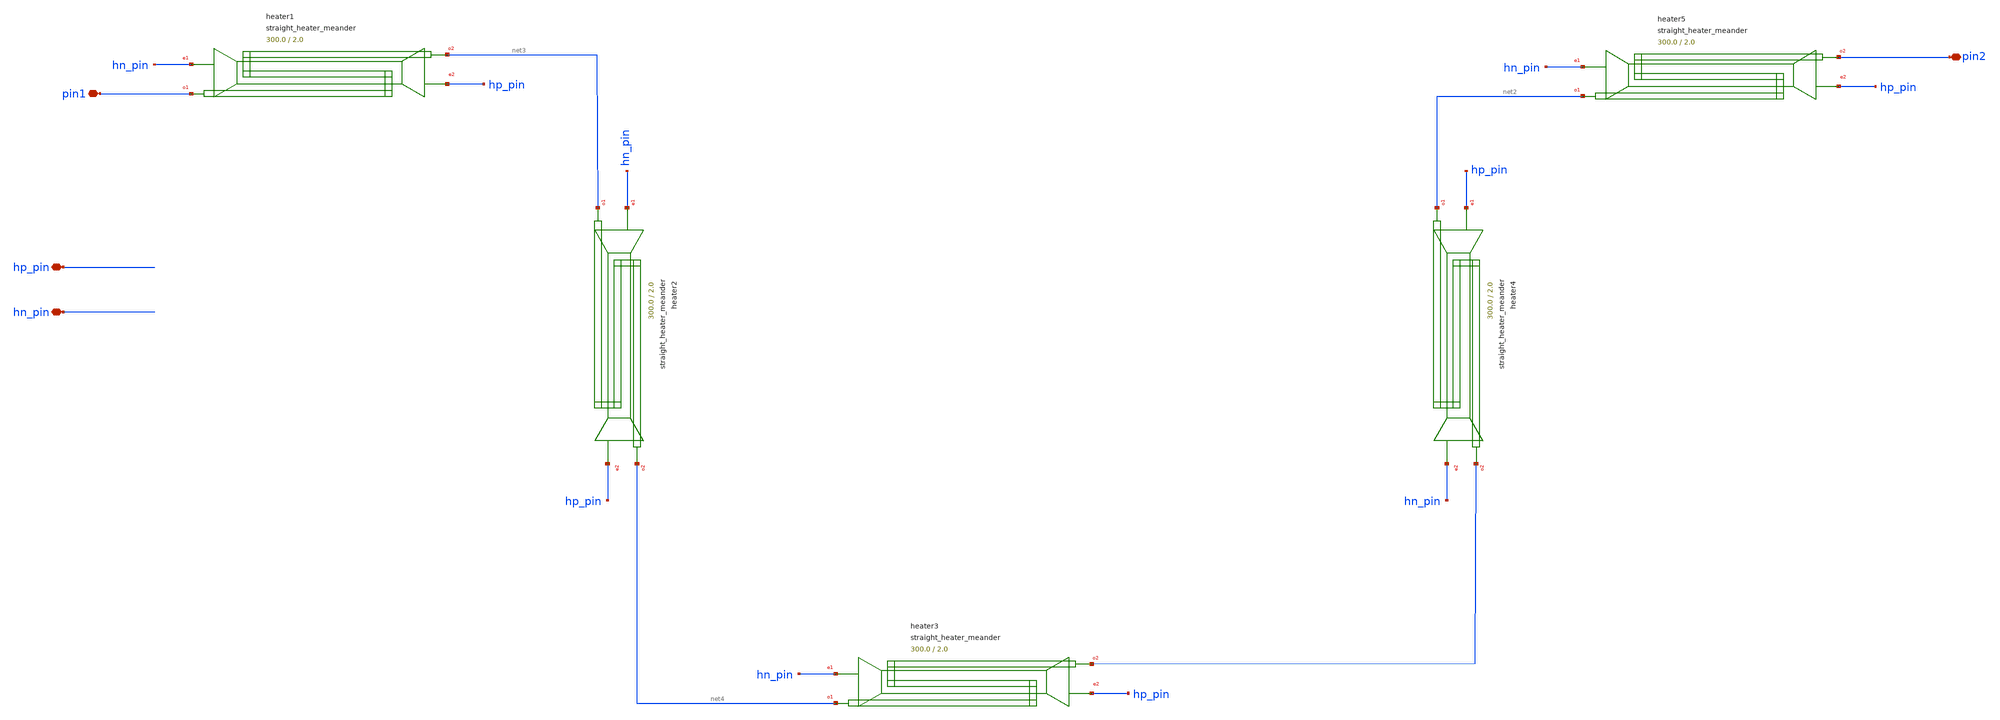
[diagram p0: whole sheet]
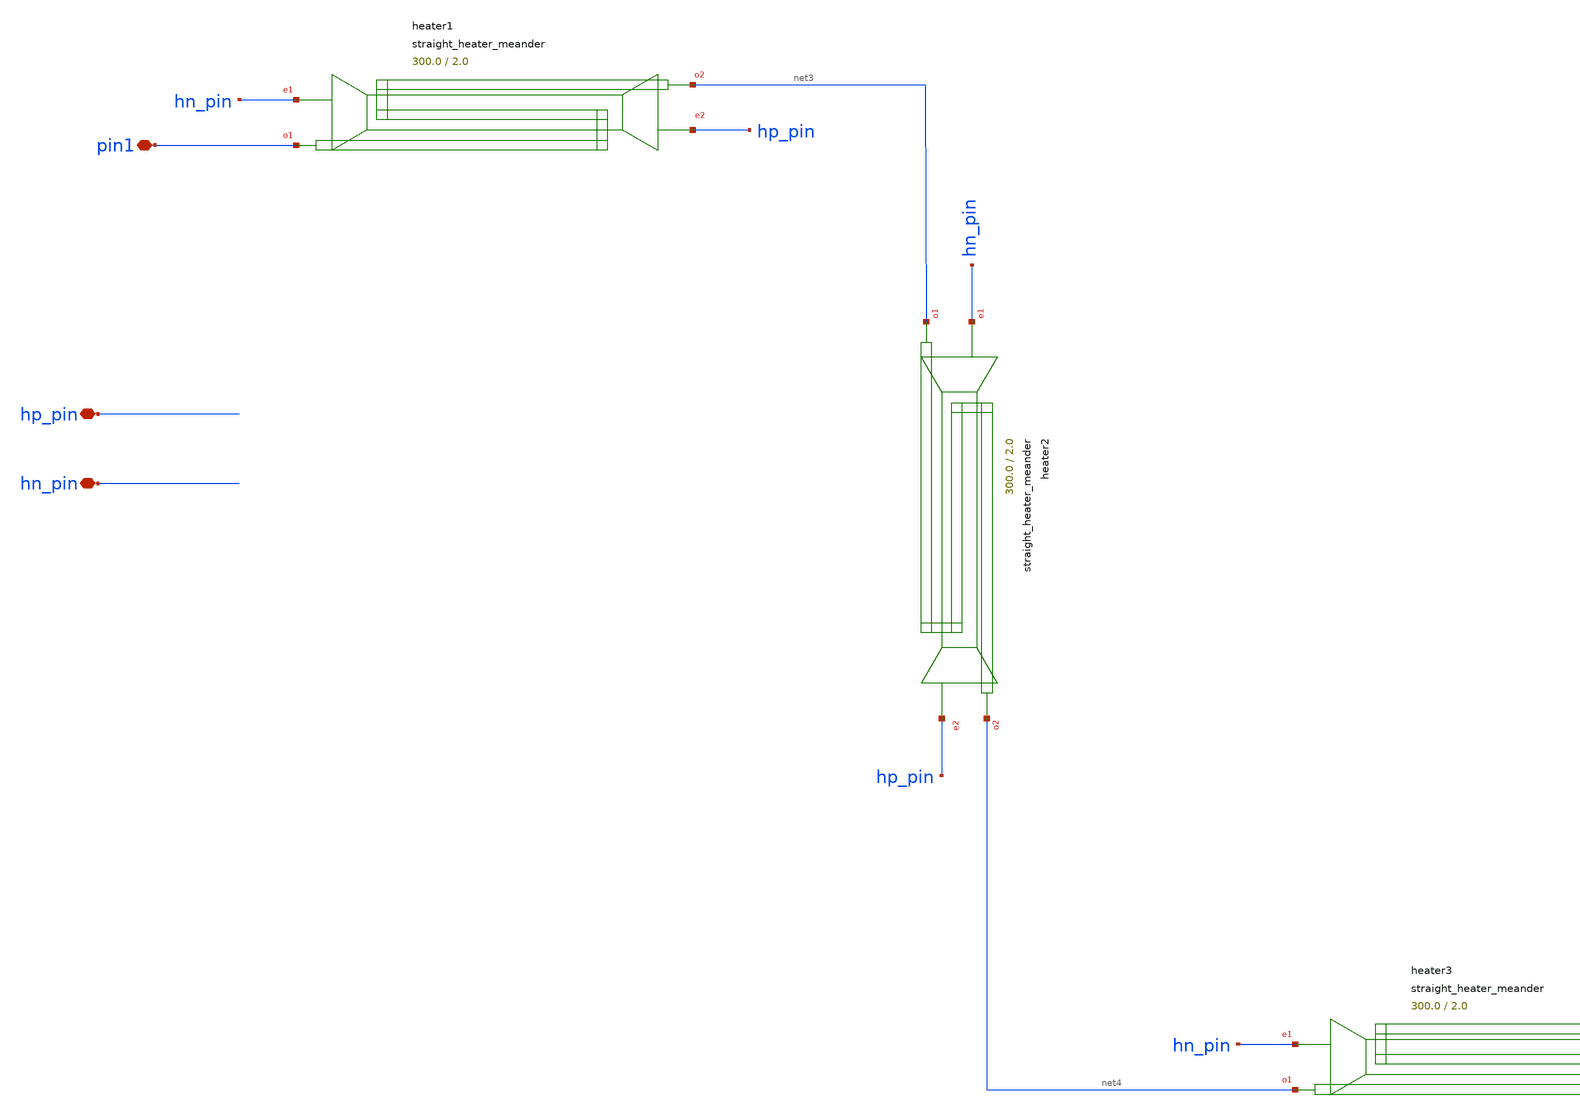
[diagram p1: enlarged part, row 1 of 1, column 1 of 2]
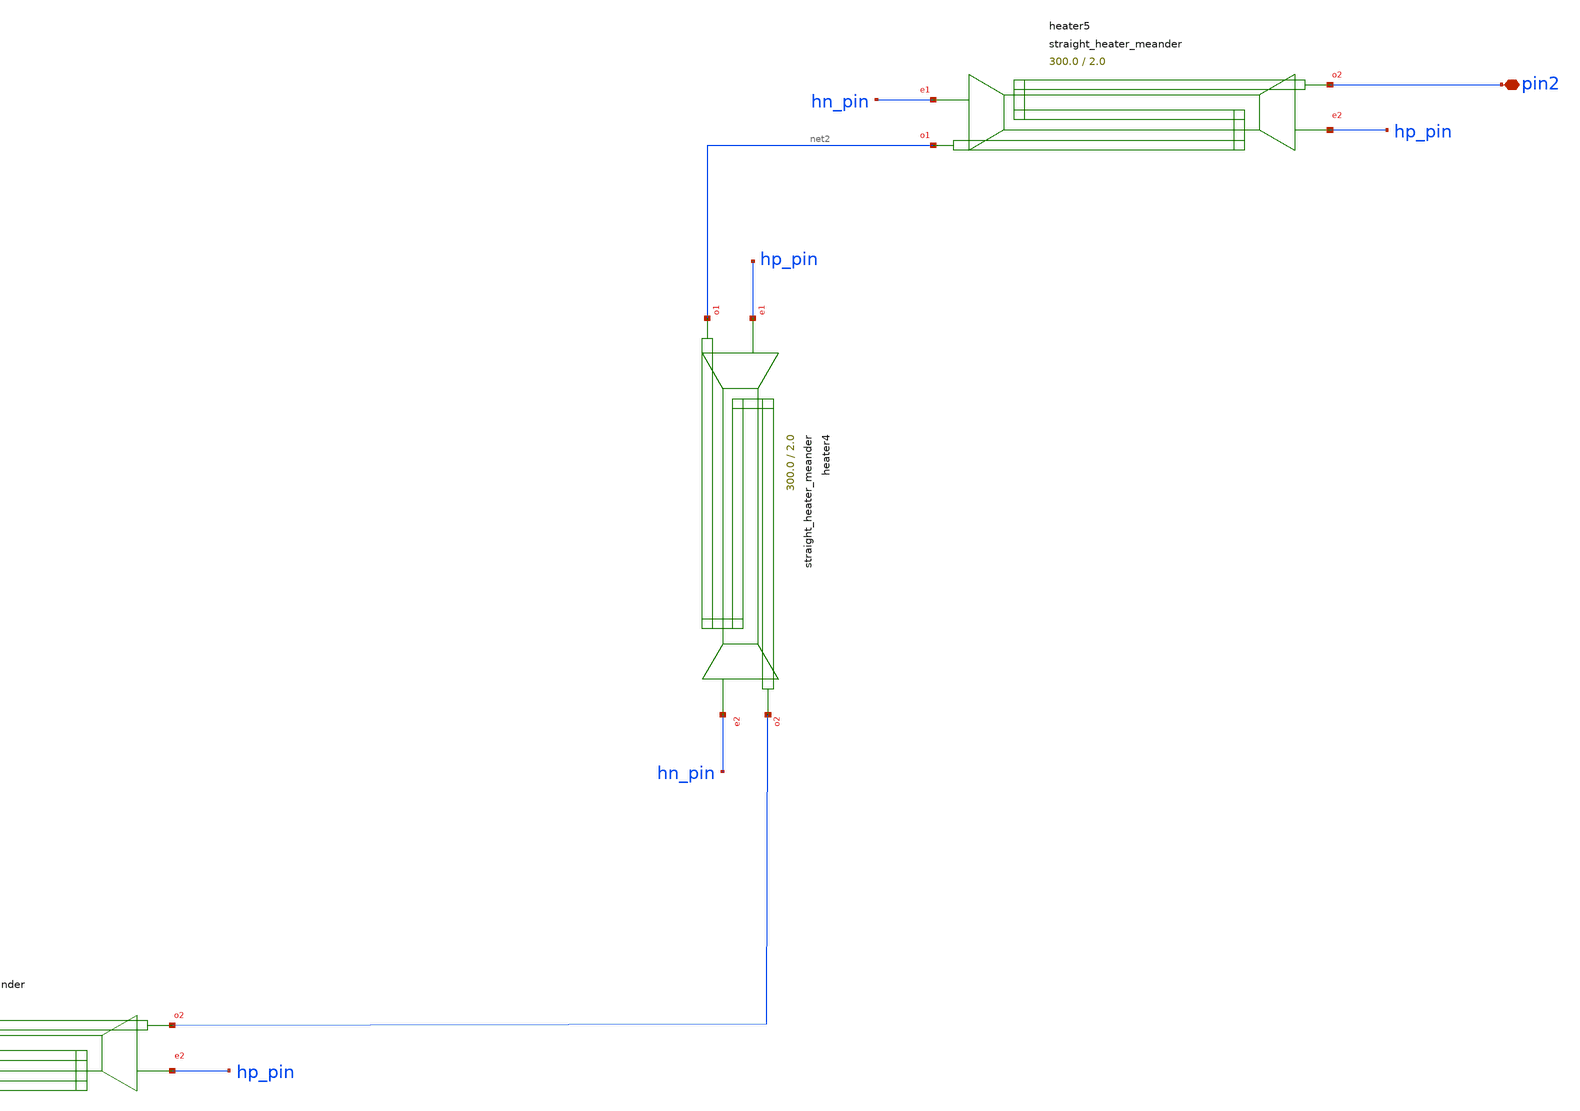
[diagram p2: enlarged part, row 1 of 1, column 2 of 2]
** sch_path: cells/xschem/tests/test_straight_heater_meander.sch
* SPDX-FileCopyrightText: 2023 Mabrains Company
* Licensed under the GNU GENERAL PUBLIC License, Version 3.0 (the "License");
* you may not use this file except in compliance with the License.
* GNU GENERAL PUBLIC LICENSE
* Version 3, 29 June 2007
* This program is free software: you can redistripute it and/or modify
* it under the terms of the GNU General Public License as published
* by the Free Software Foundation, either 3 of the License, or
* (at your option) any later version.
* This program is distriputed in the hope that it will be useful,
* but WITHOUT ANY WARRANTY; without even the implied warranty of
* MERCHANTABILITY or FITNESS FOR A PARTICULAR PURPOSE.  See the
* GNU General Public License for more details.
* You should have received a copy of the GNU General Public License
* along with this program.  If not, see <https://www.gnu.org/licenses/>.
* SPDX-License-Identifier: GPL-3.0
**.subckt test_straight_heater_meander pin1 pin2 hp_pin hn_pin
*.iopin pin1
*.iopin pin2
*.iopin hp_pin
*.iopin hn_pin
Pheater1 pin1 hn_pin net3 hp_pin straight_heater_meander length=300.0 spacing=2.0 heater_width=2.5
+ extension_length=15.0 radius=90 heater_taper_length=10.0 taper_length=10.0
Pheater2 net3 hn_pin net4 hp_pin straight_heater_meander length=300.0 spacing=2.0 heater_width=2.5
+ extension_length=15.0 radius=90 heater_taper_length=10.0 taper_length=10.0
Pheater3 net4 hn_pin net1 hp_pin straight_heater_meander length=300.0 spacing=2.0 heater_width=2.5
+ extension_length=15.0 radius=90 heater_taper_length=10.0 taper_length=10.0
Pheater4 net2 hp_pin net1 hn_pin straight_heater_meander length=300.0 spacing=2.0 heater_width=2.5
+ extension_length=15.0 radius=90 heater_taper_length=10.0 taper_length=10.0
Pheater5 net2 hn_pin pin2 hp_pin straight_heater_meander length=300.0 spacing=2.0 heater_width=2.5
+ extension_length=15.0 radius=90 heater_taper_length=10.0 taper_length=10.0
**.ends
.end
